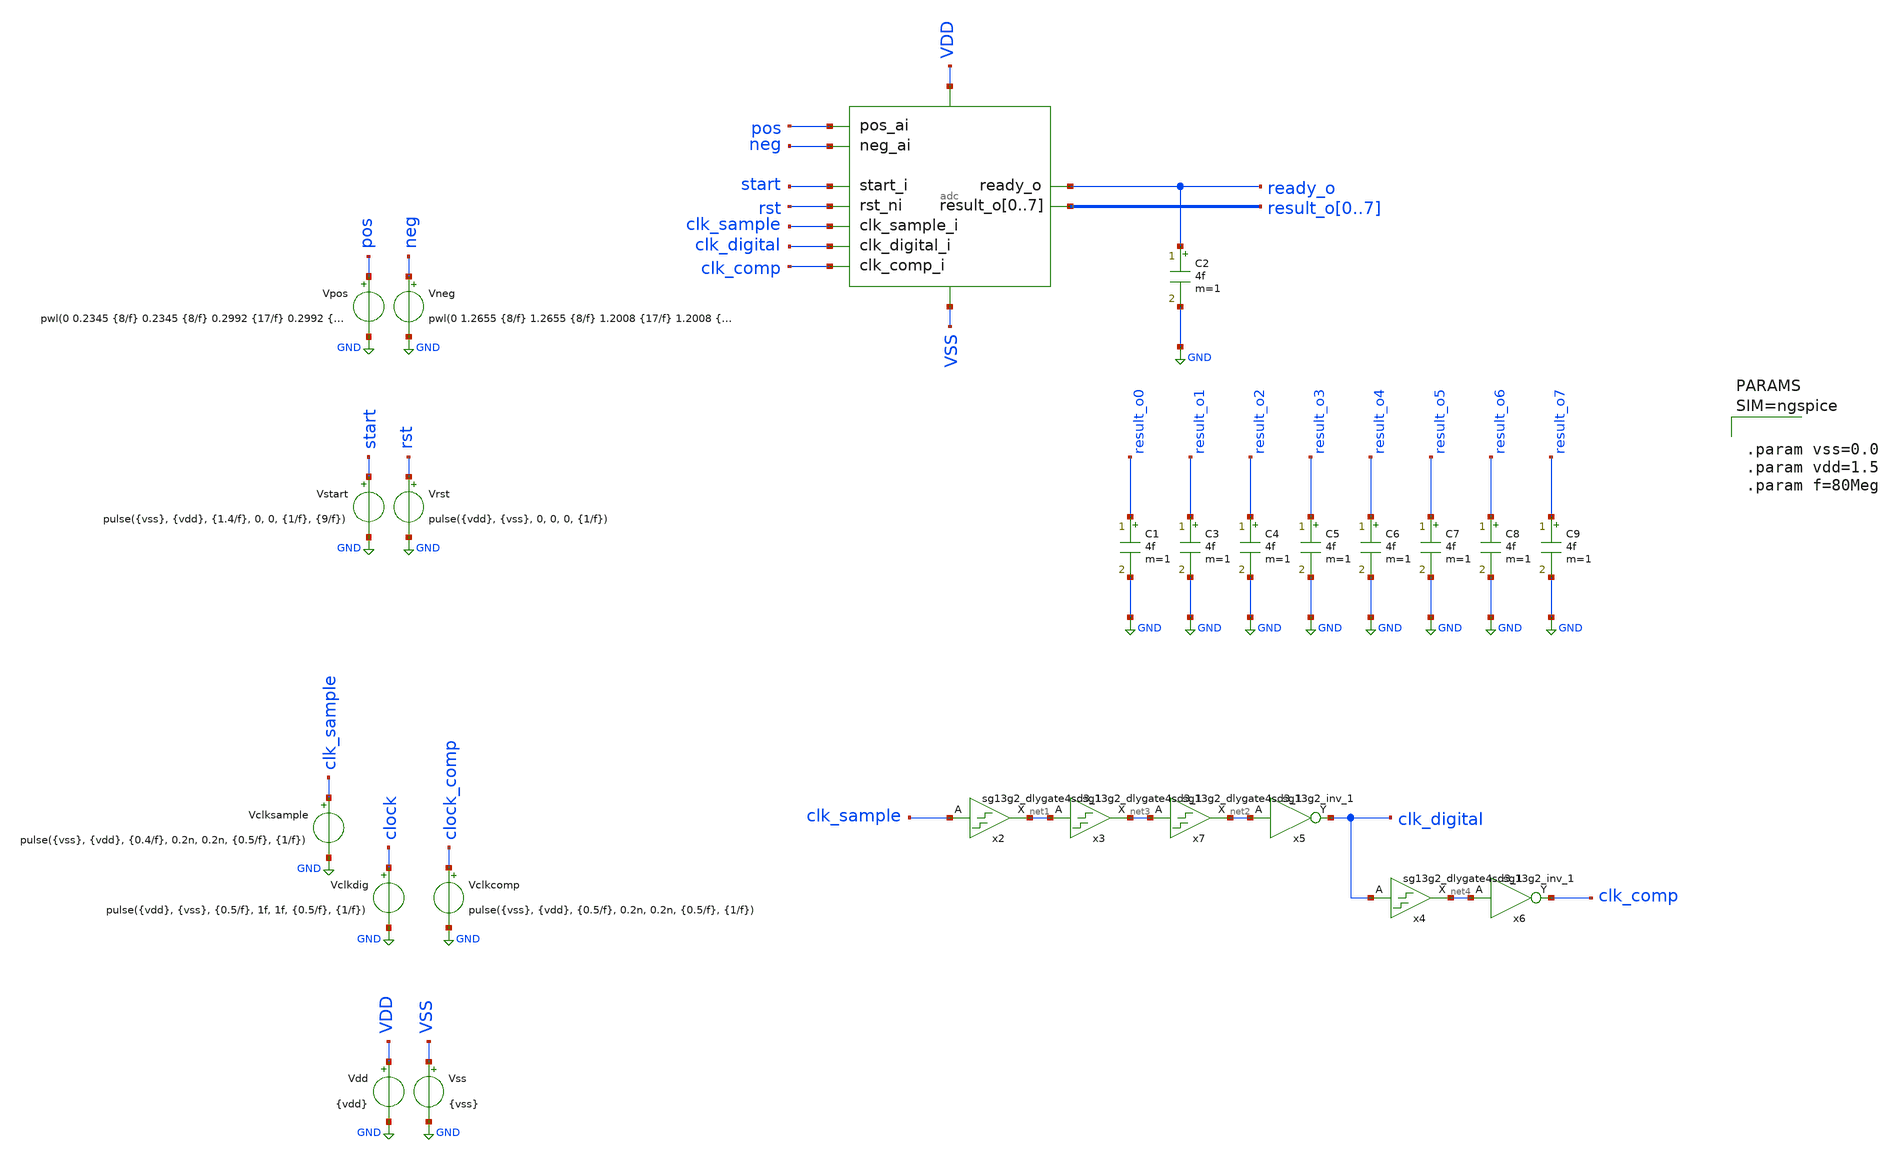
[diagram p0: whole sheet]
** sch_path: xschem/adc_tb.sch
* IHP-GmbH/IHP-Open-PDK/ihp-sg13g2/libs.tech/xschem/sg13g2_stdcells/sg13g2_buf_1.sch:
* Copyright 2023 IHP PDK Authors
* Licensed under the Apache License, Version 2.0 (the "License");
**.subckt adc_tb
x1 pos start rst clk_digital result_o0 result_o1 result_o2 result_o3 result_o4 result_o5 result_o6
+ result_o7 ready_o VDD VSS clk_comp neg clk_sample adc
Vclkdig clock GND pulse({vdd}, {vss}, {0.5/f}, 1f, 1f, {0.5/f}, {1/f})
Vrst rst GND pulse({vdd}, {vss}, 0, 0, 0, {1/f})
Vstart start GND pulse({vss}, {vdd}, {1.4/f}, 0, 0, {1/f}, {9/f})
Vpos pos GND pwl(0 0.2345 {8/f} 0.2345 {8/f} 0.2992 {17/f} 0.2992 {17/f} 0.3639 {26/f} 0.3639 {26/f}
+ 0.4286 {35/f} 0.4286 {35/f} 0.4933 {44/f} 0.4933 {44/f} 0.5580 {53/f} 0.5580 {53/f} 0.6227 {62/f} 0.6227
+ {62/f} 0.6875 {71/f} 0.6875 {71/f} 0.7522 {80/f} 0.7522 {80/f} 0.8169 {89/f} 0.8169 {89/f} 0.8816 {98/f}
+ 0.8816 {98/f} 0.9463 {107/f} 0.9463 {107/f} 1.0110 {116/f} 1.0110 {116/f} 1.0757 {125/f} 1.0757 {125/f}
+ 1.1404 {134/f} 1.1404 {134/f} 1.2051 {143/f} 1.2051 {143/f} 1.2698 {152/f} 1.2698)
.save i(vpos)
Vdd VDD GND {vdd}
Vss VSS GND {vss}
C1 result_o0 GND 4f m=1
C2 ready_o GND 4f m=1
C3 result_o1 GND 4f m=1
C4 result_o2 GND 4f m=1
C5 result_o3 GND 4f m=1
Vclkcomp clock_comp GND pulse({vss}, {vdd}, {0.5/f}, 0.2n, 0.2n, {0.5/f}, {1/f})
C6 result_o4 GND 4f m=1
C7 result_o5 GND 4f m=1
C8 result_o6 GND 4f m=1
C9 result_o7 GND 4f m=1
Vneg neg GND pwl(0 1.2655 {8/f} 1.2655 {8/f} 1.2008 {17/f} 1.2008 {17/f} 1.1361 {26/f} 1.1361 {26/f}
+ 1.0714 {35/f} 1.0714 {35/f} 1.0067 {44/f} 1.0067 {44/f} 0.9420 {53/f} 0.9420 {53/f} 0.8773 {62/f} 0.8773
+ {62/f} 0.8125 {71/f} 0.8125 {71/f} 0.7478 {80/f} 0.7478 {80/f} 0.6831 {89/f} 0.6831 {89/f} 0.6184 {98/f}
+ 0.6184 {98/f} 0.5537 {107/f} 0.5537 {107/f} 0.4890 {116/f} 0.4890 {116/f} 0.4243 {125/f} 0.4243 {125/f}
+ 0.3596 {134/f} 0.3596 {134/f} 0.2949 {143/f} 0.2949 {143/f} 0.2302 {152/f} 0.2302)
.save i(vneg)
Vclksample clk_sample GND pulse({vss}, {vdd}, {0.4/f}, 0.2n, 0.2n, {0.5/f}, {1/f})
x2 net1 clk_sample VDD VSS sg13g2_dlygate4sd3_1
x3 net3 net1 VDD VSS sg13g2_dlygate4sd3_1
x5 clk_digital net2 VDD VSS sg13g2_inv_1
x6 clk_comp net4 VDD VSS sg13g2_inv_1
x7 net2 net3 VDD VSS sg13g2_dlygate4sd3_1
x4 net4 clk_digital VDD VSS sg13g2_dlygate4sd3_1
**** begin user architecture code

.lib $::SG13G2_MODELS/cornerMOSlv.lib mos_tt
.lib $::SG13G2_MODELS/cornerCAP.lib cap_typ
.include $::PDK_ROOT/ihp-sg13g2/libs.ref/sg13g2_stdcell/spice/sg13g2_stdcell.spice




*.options method=gear maxord=2
*.options reltol=1e-3 abstol=1e-10 vntol=1e-6 chgtol=1e-14
.options gmin=1e-9 rshunt=1e12

.control
  save all
  * tran 1n 2.1u
  tran 1n 70n
  write adc_tb.raw
.endc






.param vss=0.0
.param vdd=1.5
.param f=80Meg






.model adc_buff_clk adc_bridge(in_low=0.75 in_high=0.75)

.control
pre_set auto_bridge_d_out =  ( ".model auto_bridge_out bidi_bridge(direction=0 out_high=1.5
+ t_rise=0.2n t_fall=0.2n)"    "auto_bridge_out%d [ %s ] [ %s ] null auto_bridge_out" )
pre_set auto_bridge_d_in =  ( ".model auto_bridge_in bidi_bridge(direction=1 in_low=0.5 in_high=1)"
+    "auto_bridge_in%d [ %s ] [ %s ] null auto_bridge_in" )
.endc



**** end user architecture code
**.ends

* expanding   symbol:  adc.sym # of pins=11
** sym_path: xschem/adc.sym
** sch_path: xschem/adc.sch
.subckt adc pos_ai start_i rst_ni clk_digital_i result_o0 result_o1 result_o2 result_o3 result_o4
+ result_o5 result_o6 result_o7 ready_o VDD VSS clk_comp_i neg_ai clk_sample_i
*.ipin pos_ai
*.ipin clk_digital_i
*.ipin VSS
*.ipin VDD
*.ipin start_i
*.opin ready_o
*.opin result_o0,result_o1,result_o2,result_o3,result_o4,result_o5,result_o6,result_o7
*.ipin clk_comp_i
*.ipin neg_ai
*.ipin clk_sample_i
*.ipin rst_ni
x1 sample pos_ai pos VDD VSS tgate
a1 [ net1 start_i rst_ni comp_p comp_n ] [ compare_en sample_en dac_p0 dac_p1 dac_p2 dac_p3 dac_p4
+ dac_p5 dac_p6 dac_n0 dac_n1 dac_n2 dac_n3 dac_n4 dac_n5 dac_n6 ready_o result_o0 result_o1 result_o2
+ result_o3 result_o4 result_o5 result_o6 result_o7 ] adc
x2 compare pos neg comp_2 comp_1 VSS VDD comparator
x3 sample neg_ai neg VDD VSS tgate
x4 pos neg VSS VDD dac_p0 dac_p1 dac_p2 dac_p3 dac_p4 dac_p5 dac_p6 dac_n0 dac_n1 dac_n2 dac_n3
+ dac_n4 dac_n5 dac_n6 cdac
XM5 comp_p comp_1 VSS VSS sg13_lv_nmos w=1.5u l=0.13u ng=1 m=1 mm_ok=1
XM6 comp_p comp_1 VDD VDD sg13_lv_pmos w=0.15u l=0.13u ng=1 m=1 mm_ok=1
XM7 comp_n comp_2 VSS VSS sg13_lv_nmos w=1.5u l=0.13u ng=1 m=1 mm_ok=1
XM8 comp_n comp_2 VDD VDD sg13_lv_pmos w=0.15u l=0.13u ng=1 m=1 mm_ok=1
x6 sample net2 net3 net2 rst_ni VDD VSS sg13g2_dfrbp_1
x5 net3 clk_sample_i sample_en VDD VSS sg13g2_and2_1
A2 [ clk_digital_i ] [ net1 ] adc_buff_clk
x7 compare clk_comp_i compare_en VDD VSS sg13g2_and2_1
.ends


* expanding   symbol:  sg13g2_stdcells/sg13g2_dlygate4sd3_1.sym # of pins=2
** sym_path: sg13g2_stdcells/sg13g2_dlygate4sd3_1.sym
** sch_path: sg13g2_stdcells/sg13g2_dlygate4sd3_1.sch
.subckt sg13g2_dlygate4sd3_1 X A VDD VSS
*.ipin A
*.opin X
*.iopin VDD
*.iopin VSS
XM1 net3 A VSS VSS sg13_lv_nmos w=420.00n l=130.00n ng=1 m=1 mm_ok=1
XM2 net1 net3 VSS VSS sg13_lv_nmos w=420.00n l=500.0n ng=1 m=1 mm_ok=1
XM3 net2 net1 VSS VSS sg13_lv_nmos w=420.00n l=500.0n ng=1 m=1 mm_ok=1
XM4 X net2 VSS VSS sg13_lv_nmos w=740.00n l=130.00n ng=1 m=1 mm_ok=1
XM5 net3 A VDD VDD sg13_lv_pmos w=420.00n l=130.00n ng=1 m=1 mm_ok=1
XM6 net1 net3 VDD VDD sg13_lv_pmos w=1.000u l=500.0n ng=1 m=1 mm_ok=1
XM7 net2 net1 VDD VDD sg13_lv_pmos w=1.000u l=500.0n ng=1 m=1 mm_ok=1
XM8 X net2 VDD VDD sg13_lv_pmos w=1.12u l=130.00n ng=1 m=1 mm_ok=1
.ends


* expanding   symbol:  sg13g2_stdcells/sg13g2_inv_1.sym # of pins=2
** sym_path: sg13g2_stdcells/sg13g2_inv_1.sym
** sch_path: sg13g2_stdcells/sg13g2_inv_1.sch
.subckt sg13g2_inv_1 Y A VDD VSS
*.opin Y
*.ipin A
*.iopin VDD
*.iopin VSS
XM1 Y A VSS VSS sg13_lv_nmos w=740.00n l=130.00n ng=1 m=1 mm_ok=1
XM2 Y A VDD VDD sg13_lv_pmos w=1.12u l=130.00n ng=1 m=1 mm_ok=1
.ends


* expanding   symbol:  ./tgate.sym # of pins=5
** sym_path: xschem/tgate.sym
** sch_path: xschem/tgate.sch
.subckt tgate CTRL A B VDD VSS
*.ipin CTRL
*.ipin VDD
*.ipin VSS
*.iopin B
*.iopin A
x1 ctrl_ni CTRL VDD VSS sg13g2_inv_1
x2 ctrl_i CTRL VDD VSS sg13g2_buf_1
XM3 B ctrl_i A VSS sg13_lv_nmos w=3.41u l=0.13u ng=1 m=1 mm_ok=1
XM1 A ctrl_ni B VDD sg13_lv_pmos w=8.82u l=0.13u ng=1 m=1 mm_ok=1
.ends


* expanding   symbol:  ./comparator.sym # of pins=7
** sym_path: xschem/comparator.sym
** sch_path: xschem/comparator.sch
.subckt comparator CLK IN1 IN2 OUT2 OUT1 VSS VDD
*.ipin CLK
*.ipin IN1
*.ipin IN2
*.opin OUT2
*.opin OUT1
*.ipin VSS
*.ipin VDD
XM1 P CLK VDD VDD sg13_lv_pmos w=2u l=0.13u ng=1 m=1 mm_ok=1
XM3 OUT1 OUT2 VDD VDD sg13_lv_pmos w=1u l=0.13u ng=1 m=1 mm_ok=1
XM4 OUT2 OUT1 VDD VDD sg13_lv_pmos w=1u l=0.13u ng=1 m=1 mm_ok=1
XM8 OUT1 OUT2 P VSS sg13_lv_nmos w=1u l=0.13u ng=1 m=1 mm_ok=1
XM9 P IN1 S VSS sg13_lv_nmos w=12u l=0.13u ng=6 m=1 mm_ok=1
XM11 S CLK VSS VSS sg13_lv_nmos w=4u l=2u ng=2 m=1 mm_ok=1
XM10 N IN2 S VSS sg13_lv_nmos w=12u l=0.13u ng=6 m=1 mm_ok=1
XM2 OUT1 CLK VDD VDD sg13_lv_pmos w=2u l=0.13u ng=1 m=1 mm_ok=1
XM5 N CLK VDD VDD sg13_lv_pmos w=2u l=0.13u ng=1 m=1 mm_ok=1
XM6 OUT2 CLK VDD VDD sg13_lv_pmos w=2u l=0.13u ng=1 m=1 mm_ok=1
XM7 OUT2 OUT1 N VSS sg13_lv_nmos w=1u l=0.13u ng=1 m=1 mm_ok=1
XC2 OUT1 VSS cap_cmim w=1.8e-6 l=1.8e-6 m=1 mm_ok=1
XC4 OUT2 VSS cap_cmim w=1.8e-6 l=1.8e-6 m=1 mm_ok=1
XC1 P VSS cap_cmim w=3e-6 l=3e-6 m=1 mm_ok=1
XC3 N VSS cap_cmim w=3e-6 l=3e-6 m=1 mm_ok=1
C5 S VSS 25f m=1
.ends


* expanding   symbol:  ./cdac.sym # of pins=6
** sym_path: xschem/cdac.sym
** sch_path: xschem/cdac.sch
.subckt cdac pos_ai neg_ai VSS VDD pos_ctrl_i0 pos_ctrl_i1 pos_ctrl_i2 pos_ctrl_i3 pos_ctrl_i4
+ pos_ctrl_i5 pos_ctrl_i6 neg_ctrl_i0 neg_ctrl_i1 neg_ctrl_i2 neg_ctrl_i3 neg_ctrl_i4 neg_ctrl_i5 neg_ctrl_i6
*.ipin pos_ai
*.ipin VSS
*.ipin VDD
*.ipin neg_ai
*.ipin pos_ctrl_i0,pos_ctrl_i1,pos_ctrl_i2,pos_ctrl_i3,pos_ctrl_i4,pos_ctrl_i5,pos_ctrl_i6
*.ipin neg_ctrl_i0,neg_ctrl_i1,neg_ctrl_i2,neg_ctrl_i3,neg_ctrl_i4,neg_ctrl_i5,neg_ctrl_i6
x2 net1 pos_ctrl_i0 VDD VSS sg13g2_inv_2
x3 net2 pos_ctrl_i1 VDD VSS sg13g2_inv_2
x4 net3 pos_ctrl_i2 VDD VSS sg13g2_inv_2
x5 net4 pos_ctrl_i3 VDD VSS sg13g2_inv_2
x6 net5 pos_ctrl_i4 VDD VSS sg13g2_inv_2
x7 net6 pos_ctrl_i5 VDD VSS sg13g2_inv_2
x8 net7 pos_ctrl_i6 VDD VSS sg13g2_inv_2
XC1 pos_ai net7 cap_cmim w={s} l={s} m=1 mm_ok=1
XC2 pos_ai net6 cap_cmim w={s} l={s} m=2 mm_ok=1
XC3 pos_ai net5 cap_cmim w={s} l={s} m=4 mm_ok=1
x10 net8 neg_ctrl_i0 VDD VSS sg13g2_inv_2
x11 net9 neg_ctrl_i1 VDD VSS sg13g2_inv_2
x12 net10 neg_ctrl_i2 VDD VSS sg13g2_inv_2
x13 net11 neg_ctrl_i3 VDD VSS sg13g2_inv_2
x14 net12 neg_ctrl_i4 VDD VSS sg13g2_inv_2
x15 net13 neg_ctrl_i5 VDD VSS sg13g2_inv_2
x16 net14 neg_ctrl_i6 VDD VSS sg13g2_inv_2
XC10 neg_ai net14 cap_cmim w={s} l={s} m=1 mm_ok=1
XC11 neg_ai net13 cap_cmim w={s} l={s} m=2 mm_ok=1
XC12 neg_ai net12 cap_cmim w={s} l={s} m=4 mm_ok=1
* noconn VDD
.param s=2.5292e-6
x1 net15 neg_ctrl_i0 VDD VSS sg13g2_buf_2
x9 net16 pos_ctrl_i0 VDD VSS sg13g2_buf_2
XC7 pos_ai net1 cap_cmim w={s} l={s} m=32 mm_ok=1
XC9 neg_ai net16 cap_cmim w={s} l={s} m=32 mm_ok=1
XC13 neg_ai net8 cap_cmim w={s} l={s} m=32 mm_ok=1
XC16 pos_ai net15 cap_cmim w={s} l={s} m=32 mm_ok=1
x17 net17 neg_ctrl_i1 VDD VSS sg13g2_buf_2
x18 net18 pos_ctrl_i1 VDD VSS sg13g2_buf_2
XC17 neg_ai net18 cap_cmim w={s} l={s} m=16 mm_ok=1
XC18 pos_ai net17 cap_cmim w={s} l={s} m=16 mm_ok=1
XC4 neg_ai net9 cap_cmim w={s} l={s} m=16 mm_ok=1
XC8 pos_ai net2 cap_cmim w={s} l={s} m=16 mm_ok=1
x19 net19 neg_ctrl_i2 VDD VSS sg13g2_buf_2
x20 net20 pos_ctrl_i2 VDD VSS sg13g2_buf_2
XC19 pos_ai net19 cap_cmim w={s} l={s} m=8 mm_ok=1
XC6 neg_ai net10 cap_cmim w={s} l={s} m=8 mm_ok=1
XC15 pos_ai net3 cap_cmim w={s} l={s} m=8 mm_ok=1
XC20 neg_ai net20 cap_cmim w={s} l={s} m=8 mm_ok=1
x21 net21 neg_ctrl_i3 VDD VSS sg13g2_buf_2
x22 net22 pos_ctrl_i3 VDD VSS sg13g2_buf_2
XC5 pos_ai net4 cap_cmim w={s} l={s} m=4 mm_ok=1
XC14 neg_ai net22 cap_cmim w={s} l={s} m=4 mm_ok=1
XC21 neg_ai net11 cap_cmim w={s} l={s} m=4 mm_ok=1
XC22 pos_ai net21 cap_cmim w={s} l={s} m=4 mm_ok=1
XC23 neg_ai VSS cap_cmim w={s} l={s} m=47.54545455 mm_ok=1
XC24 pos_ai VSS cap_cmim w={s} l={s} m=47.54545455 mm_ok=1
.ends


* expanding   symbol:  sg13g2_stdcells/sg13g2_dfrbp_1.sym # of pins=5
** sym_path: sg13g2_stdcells/sg13g2_dfrbp_1.sym
** sch_path: sg13g2_stdcells/sg13g2_dfrbp_1.sch
.subckt sg13g2_dfrbp_1 Q Q_N CLK D RESET_B VDD VSS
*.ipin D
*.ipin RESET_B
*.ipin CLK
*.opin Q
*.opin Q_N
*.iopin VDD
*.iopin VSS
XM1 Db D net10 VSS sg13_lv_nmos w=420.00n l=130.00n ng=1 m=1 mm_ok=1
XM2 net10 RESET_B VSS VSS sg13_lv_nmos w=420.00n l=130.00n ng=1 m=1 mm_ok=1
XM3 net1 clkneg net9 VSS sg13_lv_nmos w=420.00n l=130.00n ng=1 m=1 mm_ok=1
XM4 net9 net1 VSS VSS sg13_lv_nmos w=420.00n l=130.00n ng=1 m=1 mm_ok=1
XM5 net1 net1 net5 VSS sg13_lv_nmos w=420.00n l=130.00n ng=1 m=1 mm_ok=1
XM6 net5 RESET_B VSS VSS sg13_lv_nmos w=420.00n l=130.00n ng=1 m=1 mm_ok=1
XM7 Q_N net1 VSS VSS sg13_lv_nmos w=740.00n l=130.00n ng=1 m=1 mm_ok=1
XM8 net2 net1 VSS VSS sg13_lv_nmos w=740.00n l=130.00n ng=1 m=1 mm_ok=1
XM9 Q net2 VSS VSS sg13_lv_nmos w=740.00n l=130.00n ng=1 m=1 mm_ok=1
XM10 clkneg CLK VSS VSS sg13_lv_nmos w=740.00n l=130.00n ng=1 m=1 mm_ok=1
XM11 clkpos clkneg VSS VSS sg13_lv_nmos w=740.00n l=130.00n ng=1 m=1 mm_ok=1
XM12 Db clkneg net3 VSS sg13_lv_nmos w=420.00n l=130.00n ng=1 m=1 mm_ok=1
XM13 net3 clkpos net8 VSS sg13_lv_nmos w=420.00n l=130.00n ng=1 m=1 mm_ok=1
XM14 net8 net3 net4 VSS sg13_lv_nmos w=420.00n l=130.00n ng=1 m=1 mm_ok=1
XM15 net4 RESET_B VSS VSS sg13_lv_nmos w=420.00n l=130.00n ng=1 m=1 mm_ok=1
XM16 net3 net3 VSS VSS sg13_lv_nmos w=740.00n l=130.00n ng=1 m=1 mm_ok=1
XM17 net3 clkpos net1 VSS sg13_lv_nmos w=740.00n l=130.00n ng=1 m=1 mm_ok=1
XM18 Db RESET_B VDD VDD sg13_lv_pmos w=420.00n l=130.00n ng=1 m=1 mm_ok=1
XM19 Db D VDD VDD sg13_lv_pmos w=420.00n l=130.00n ng=1 m=1 mm_ok=1
XM20 net7 net1 VDD VDD sg13_lv_pmos w=420.00n l=130.00n ng=1 m=1 mm_ok=1
XM21 net1 clkpos net7 VDD sg13_lv_pmos w=420.00n l=130.00n ng=1 m=1 mm_ok=1
XM22 net1 net1 VDD VDD sg13_lv_pmos w=420.00n l=130.00n ng=1 m=1 mm_ok=1
XM23 net1 RESET_B VDD VDD sg13_lv_pmos w=420.00n l=130.00n ng=1 m=1 mm_ok=1
XM24 Q_N net1 VDD VDD sg13_lv_pmos w=1.12u l=130.00n ng=1 m=1 mm_ok=1
XM25 net2 net1 VDD VDD sg13_lv_pmos w=1.12u l=130.00n ng=1 m=1 mm_ok=1
XM26 Q net2 VDD VDD sg13_lv_pmos w=1.12u l=130.00n ng=1 m=1 mm_ok=1
XM27 clkneg CLK VDD VDD sg13_lv_pmos w=1.12u l=130.00n ng=1 m=1 mm_ok=1
XM28 clkpos clkneg VDD VDD sg13_lv_pmos w=1.12u l=130.00n ng=1 m=1 mm_ok=1
XM29 Db clkpos net3 VDD sg13_lv_pmos w=420.00n l=130.00n ng=1 m=1 mm_ok=1
XM30 net6 net3 VDD VDD sg13_lv_pmos w=420.00n l=130.00n ng=1 m=1 mm_ok=1
XM31 net3 clkneg net6 VDD sg13_lv_pmos w=420.00n l=130.00n ng=1 m=1 mm_ok=1
XM32 net3 RESET_B VDD VDD sg13_lv_pmos w=420.00n l=130.00n ng=1 m=1 mm_ok=1
XM33 net3 net3 VDD VDD sg13_lv_pmos w=1.000u l=130.00n ng=1 m=1 mm_ok=1
XM34 net3 clkneg net1 VDD sg13_lv_pmos w=1.000u l=130.00n ng=1 m=1 mm_ok=1
.ends


* expanding   symbol:  sg13g2_stdcells/sg13g2_and2_1.sym # of pins=3
** sym_path: sg13g2_stdcells/sg13g2_and2_1.sym
** sch_path: sg13g2_stdcells/sg13g2_and2_1.sch
.subckt sg13g2_and2_1 X A B VDD VSS
*.ipin A
*.ipin B
*.opin X
*.iopin VDD
*.iopin VSS
XM1 net1 A net2 VSS sg13_lv_nmos w=640.00n l=130.00n ng=1 m=1 mm_ok=1
XM2 net2 B VSS VSS sg13_lv_nmos w=640.00n l=130.00n ng=1 m=1 mm_ok=1
XM3 X net1 VSS VSS sg13_lv_nmos w=740.00n l=130.00n ng=1 m=1 mm_ok=1
XM4 net1 B VDD VDD sg13_lv_pmos w=840.00n l=130.00n ng=1 m=1 mm_ok=1
XM5 net1 A VDD VDD sg13_lv_pmos w=840.00n l=130.00n ng=1 m=1 mm_ok=1
XM6 X net1 VDD VDD sg13_lv_pmos w=1.12u l=130.00n ng=1 m=1 mm_ok=1
.ends


* expanding   symbol:  sg13g2_stdcells/sg13g2_buf_1.sym # of pins=2
** sym_path: sg13g2_stdcells/sg13g2_buf_1.sym
** sch_path: sg13g2_stdcells/sg13g2_buf_1.sch
.subckt sg13g2_buf_1 X A VDD VSS
*.ipin A
*.opin X
*.iopin VDD
*.iopin VSS
XM1 net1 A VSS VSS sg13_lv_nmos w=550.00n l=130.00n ng=1 m=1 mm_ok=1
XM2 X net1 VSS VSS sg13_lv_nmos w=740.00n l=130.00n ng=1 m=1 mm_ok=1
XM3 net1 A VDD VDD sg13_lv_pmos w=840.00n l=130.00n ng=1 m=1 mm_ok=1
XM4 X net1 VDD VDD sg13_lv_pmos w=1.12u l=130.00n ng=1 m=1 mm_ok=1
.ends


* expanding   symbol:  sg13g2_stdcells/sg13g2_inv_2.sym # of pins=2
** sym_path: sg13g2_stdcells/sg13g2_inv_2.sym
** sch_path: sg13g2_stdcells/sg13g2_inv_2.sch
.subckt sg13g2_inv_2 Y A VDD VSS
*.opin Y
*.ipin A
*.iopin VDD
*.iopin VSS
XM1 Y A VSS VSS sg13_lv_nmos w=1.48u l=130.00n ng=2 m=1 mm_ok=1
XM2 Y A VDD VDD sg13_lv_pmos w=2.24u l=130.00n ng=2 m=1 mm_ok=1
.ends


* expanding   symbol:  sg13g2_stdcells/sg13g2_buf_2.sym # of pins=2
** sym_path: sg13g2_stdcells/sg13g2_buf_2.sym
** sch_path: sg13g2_stdcells/sg13g2_buf_2.sch
.subckt sg13g2_buf_2 X A VDD VSS
*.ipin A
*.opin X
*.iopin VDD
*.iopin VSS
XM1 net1 A VSS VSS sg13_lv_nmos w=640.00n l=130.00n ng=1 m=1 mm_ok=1
XM2 X net1 VSS VSS sg13_lv_nmos w=1.48u l=130.00n ng=2 m=1 mm_ok=1
XM3 net1 A VDD VDD sg13_lv_pmos w=1.000u l=130.00n ng=1 m=1 mm_ok=1
XM4 X net1 VDD VDD sg13_lv_pmos w=2.24u l=130.00n ng=2 m=1 mm_ok=1
.ends

.GLOBAL GND
**** begin user architecture code
.model adc d_cosim simulation="ivlng" sim_args=["adc"]
**** end user architecture code
.end
